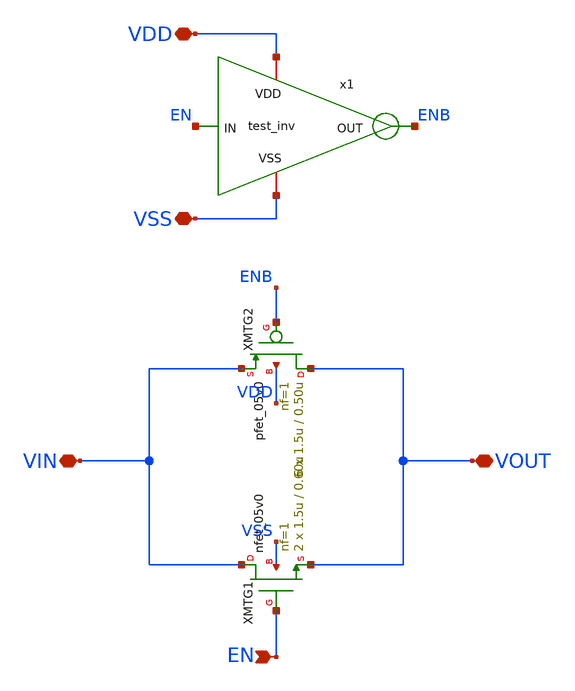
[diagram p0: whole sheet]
** sch_path: designs/libs/core_test/test_tg/test_tg.sch
**.subckt test_tg VIN VOUT EN VDD VSS
*.iopin VIN
*.iopin VOUT
*.ipin EN
*.iopin VDD
*.iopin VSS
XMTG1 VIN EN VOUT VSS nfet_05v0 L=0.60u W=1.5u nf=1 ad='int((nf+1)/2) * W/nf * 0.18u' as='int((nf+2)/2) * W/nf * 0.18u'
+ pd='2*int((nf+1)/2) * (W/nf + 0.18u)' ps='2*int((nf+2)/2) * (W/nf + 0.18u)' nrd='0.18u / W' nrs='0.18u / W'
+ sa=0 sb=0 sd=0 m=2
XMTG2 VOUT ENB VIN VDD pfet_05v0 L=0.50u W=1.5u nf=1 ad='int((nf+1)/2) * W/nf * 0.18u' as='int((nf+2)/2) * W/nf * 0.18u'
+ pd='2*int((nf+1)/2) * (W/nf + 0.18u)' ps='2*int((nf+2)/2) * (W/nf + 0.18u)' nrd='0.18u / W' nrs='0.18u / W'
+ sa=0 sb=0 sd=0 m=6
x1 VDD ENB EN VSS test_inv
**.ends

* expanding   symbol:  libs/core_test/test_inv/test_inv.sym # of pins=4
** sym_path: designs/libs/core_test/test_inv/test_inv.sym
** sch_path: designs/libs/core_test/test_inv/test_inv.sch
.subckt test_inv VDD OUT IN VSS
*.opin OUT
*.ipin IN
*.iopin VDD
*.iopin VSS
XMINV1 OUT IN VSS VSS nfet_05v0 L=0.60u W=0.42u nf=1 ad='int((nf+1)/2) * W/nf * 0.18u' as='int((nf+2)/2) * W/nf * 0.18u'
+ pd='2*int((nf+1)/2) * (W/nf + 0.18u)' ps='2*int((nf+2)/2) * (W/nf + 0.18u)' nrd='0.18u / W' nrs='0.18u / W'
+ sa=0 sb=0 sd=0 m=1
XMINV2 OUT IN VDD VDD pfet_05v0 L=0.50u W=0.60u nf=1 ad='int((nf+1)/2) * W/nf * 0.18u' as='int((nf+2)/2) * W/nf * 0.18u'
+ pd='2*int((nf+1)/2) * (W/nf + 0.18u)' ps='2*int((nf+2)/2) * (W/nf + 0.18u)' nrd='0.18u / W' nrs='0.18u / W'
+ sa=0 sb=0 sd=0 m=1
.ends

.end
